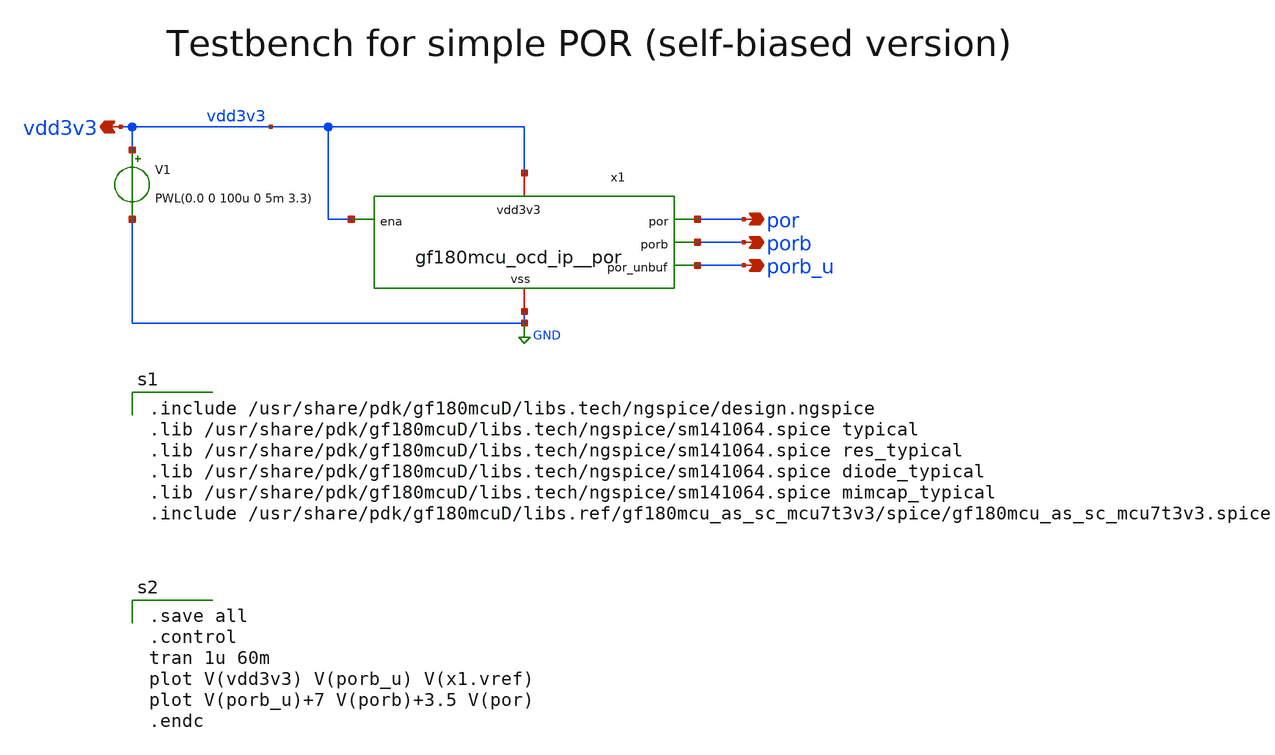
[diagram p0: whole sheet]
** sch_path: projects/programmable_transceiver_platform/analog/core_support/por/xschem/simple_por_tb2.sch
**.subckt simple_por_tb2 vdd3v3 porb_u porb por
*.opin vdd3v3
*.opin porb_u
*.opin porb
*.opin por
V1 vdd3v3 GND PWL(0.0 0 100u 0 5m 3.3)
x1 vdd3v3 vdd3v3 porb_u GND porb por gf180mcu_ocd_ip__por
**** begin user architecture code

.save all
.control
tran 1u 60m
plot V(vdd3v3) V(porb_u) V(x1.vref)
plot V(porb_u)+7 V(porb)+3.5 V(por)
.endc


.include /usr/share/pdk/gf180mcuD/libs.tech/ngspice/design.ngspice
.lib /usr/share/pdk/gf180mcuD/libs.tech/ngspice/sm141064.spice typical
.lib /usr/share/pdk/gf180mcuD/libs.tech/ngspice/sm141064.spice res_typical
.lib /usr/share/pdk/gf180mcuD/libs.tech/ngspice/sm141064.spice diode_typical
.lib /usr/share/pdk/gf180mcuD/libs.tech/ngspice/sm141064.spice mimcap_typical
.include /usr/share/pdk/gf180mcuD/libs.ref/gf180mcu_as_sc_mcu7t3v3/spice/gf180mcu_as_sc_mcu7t3v3.spice

**** end user architecture code
**.ends
.GLOBAL GND
.end
